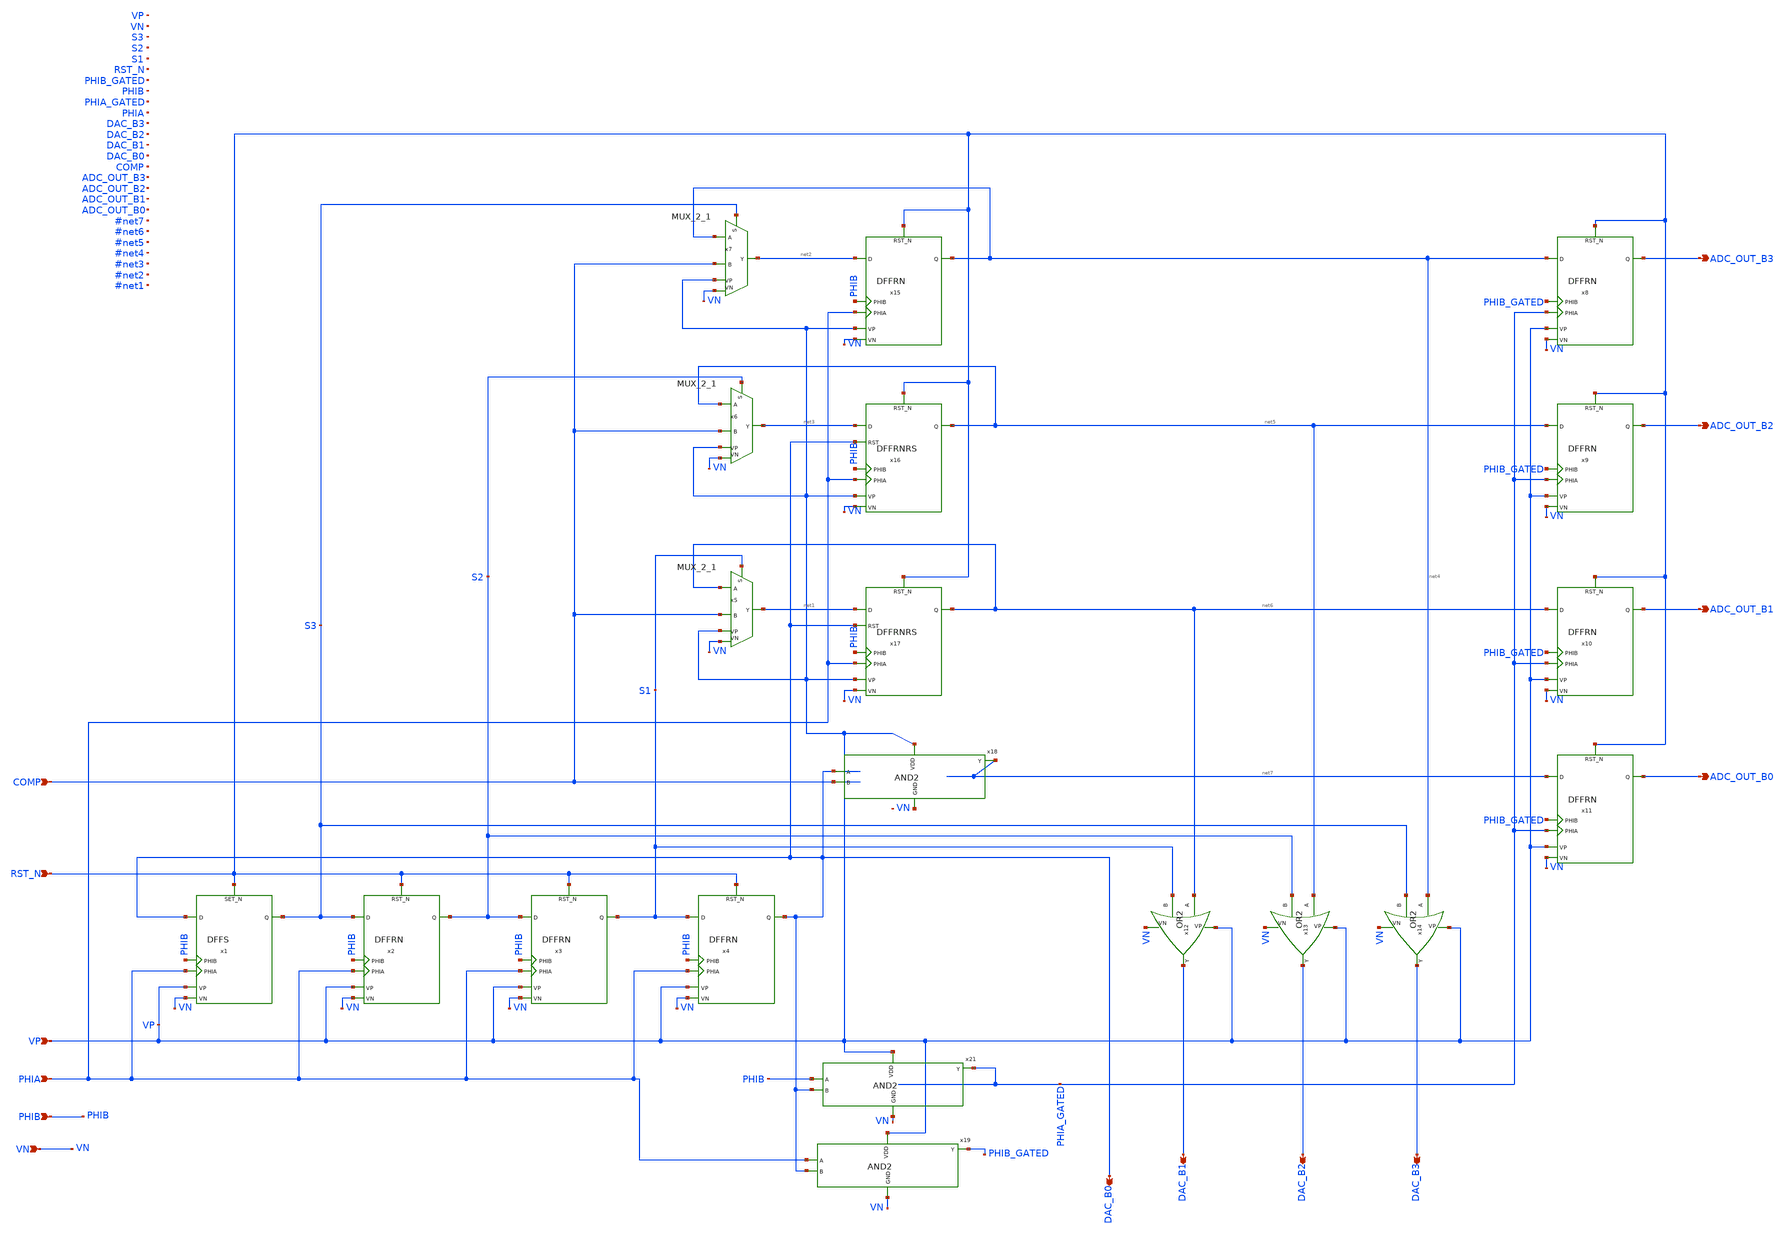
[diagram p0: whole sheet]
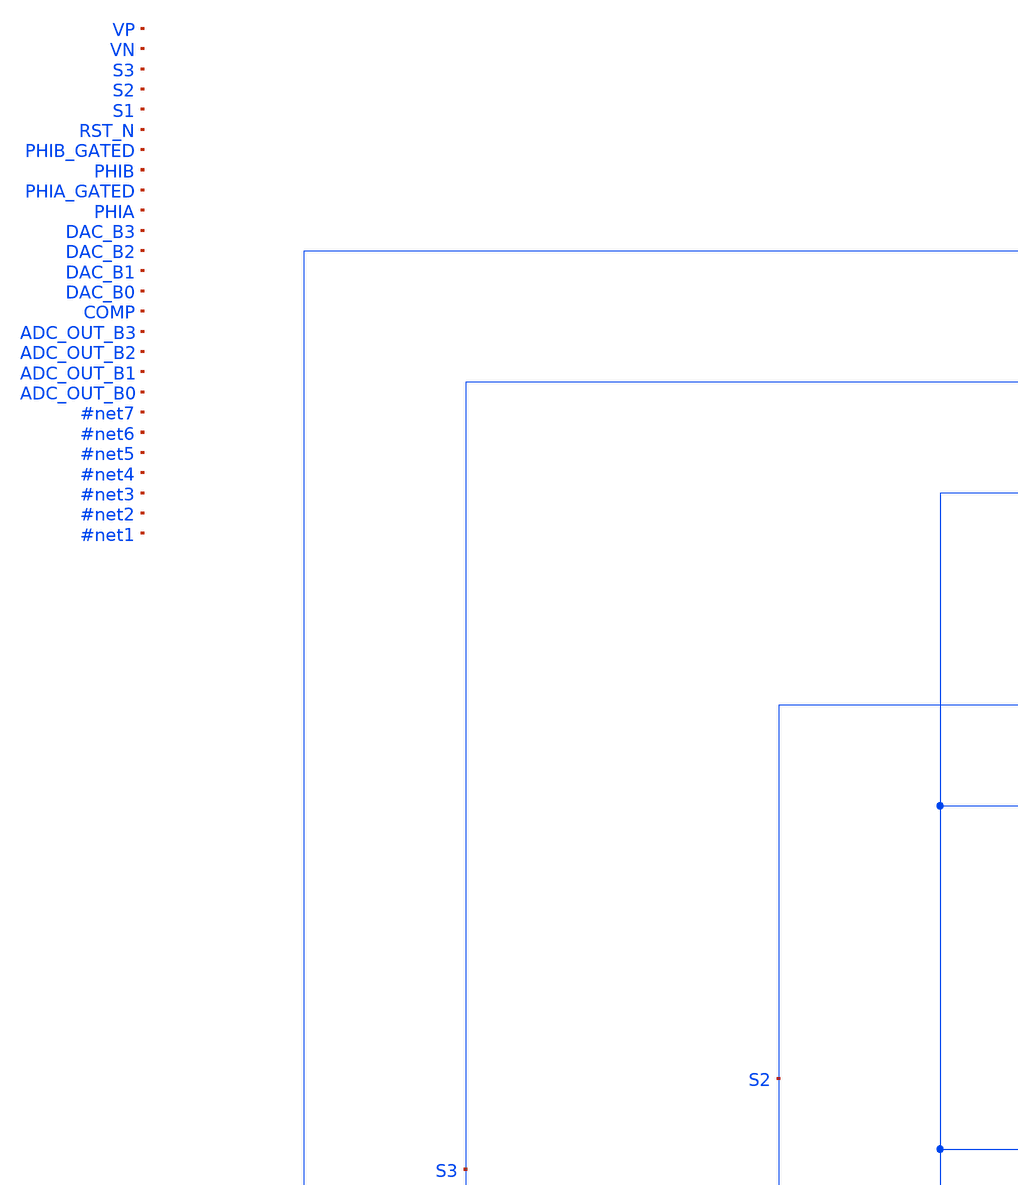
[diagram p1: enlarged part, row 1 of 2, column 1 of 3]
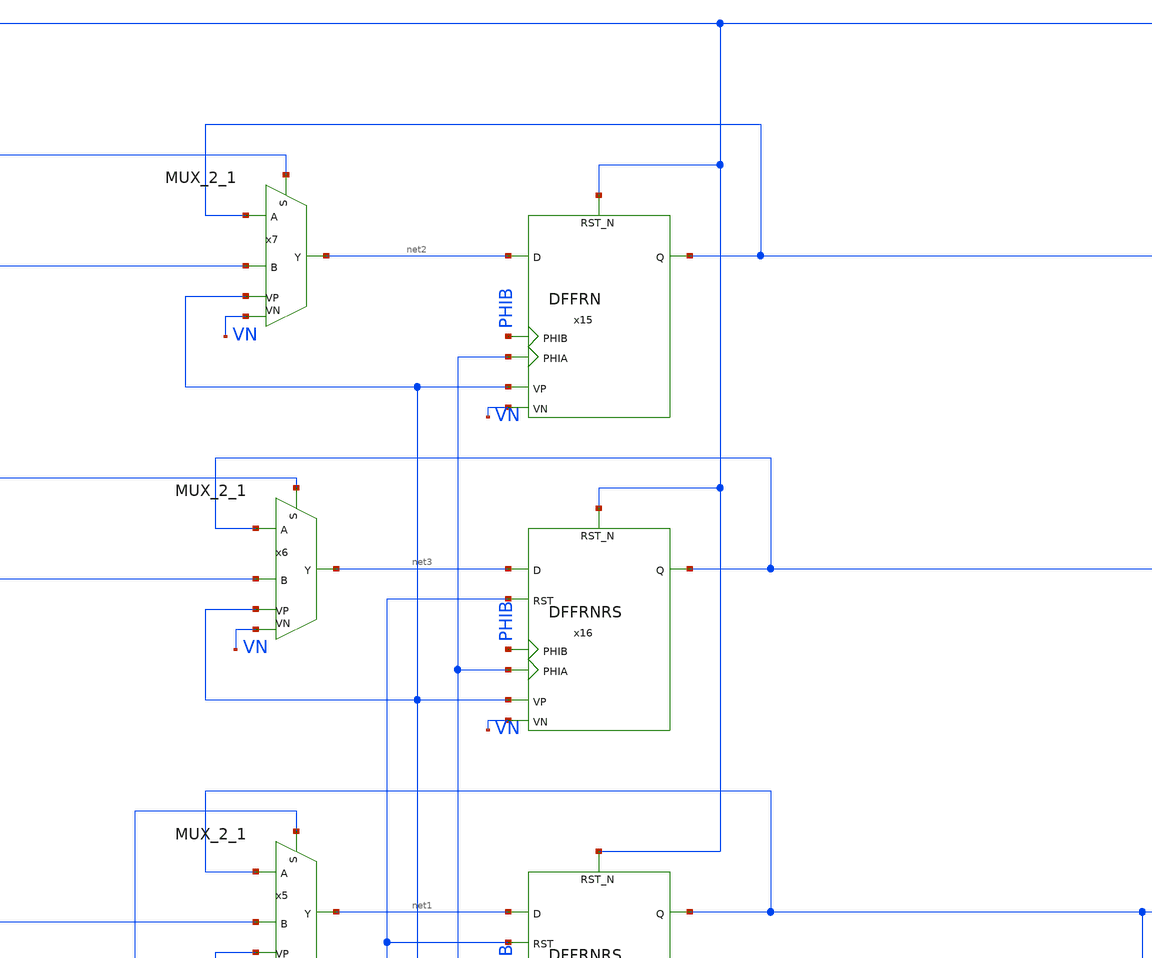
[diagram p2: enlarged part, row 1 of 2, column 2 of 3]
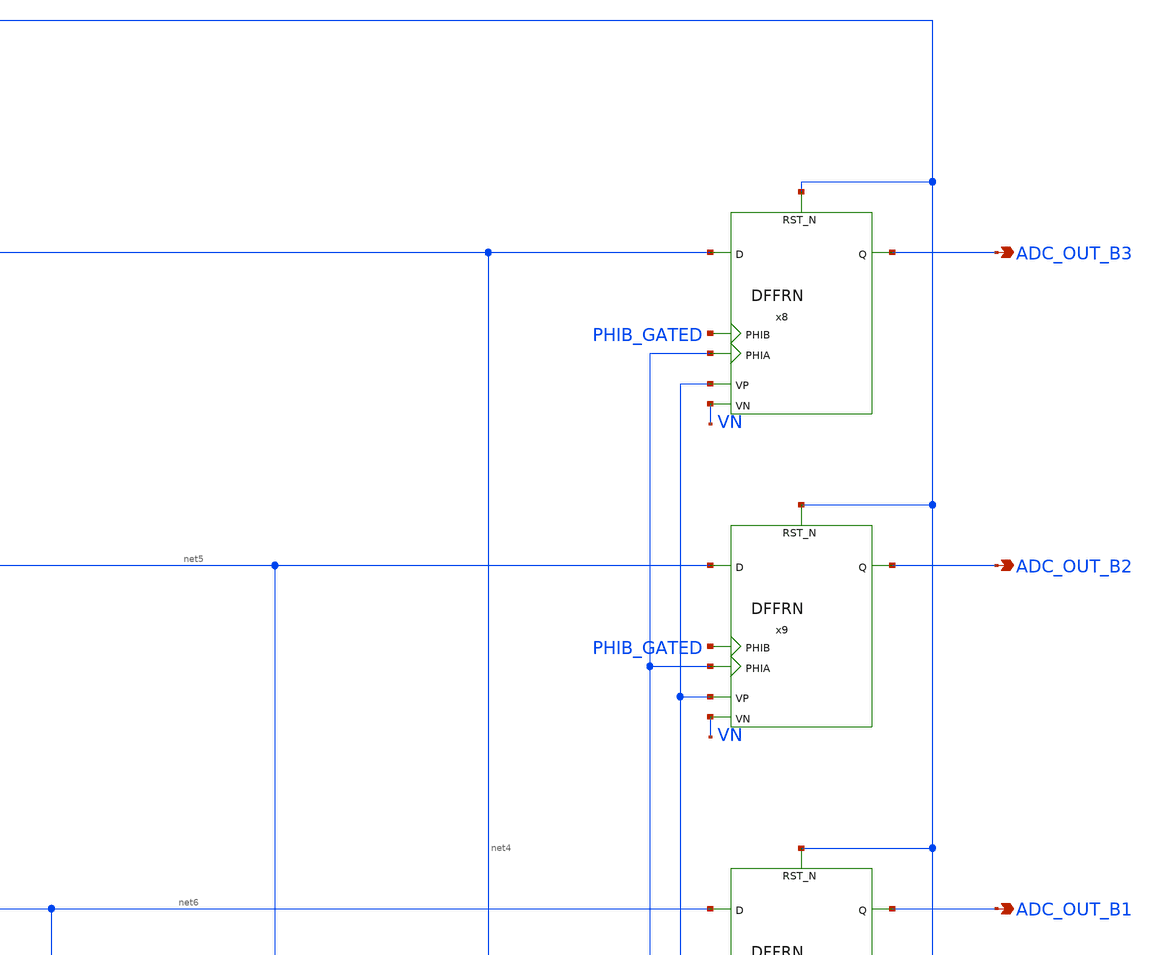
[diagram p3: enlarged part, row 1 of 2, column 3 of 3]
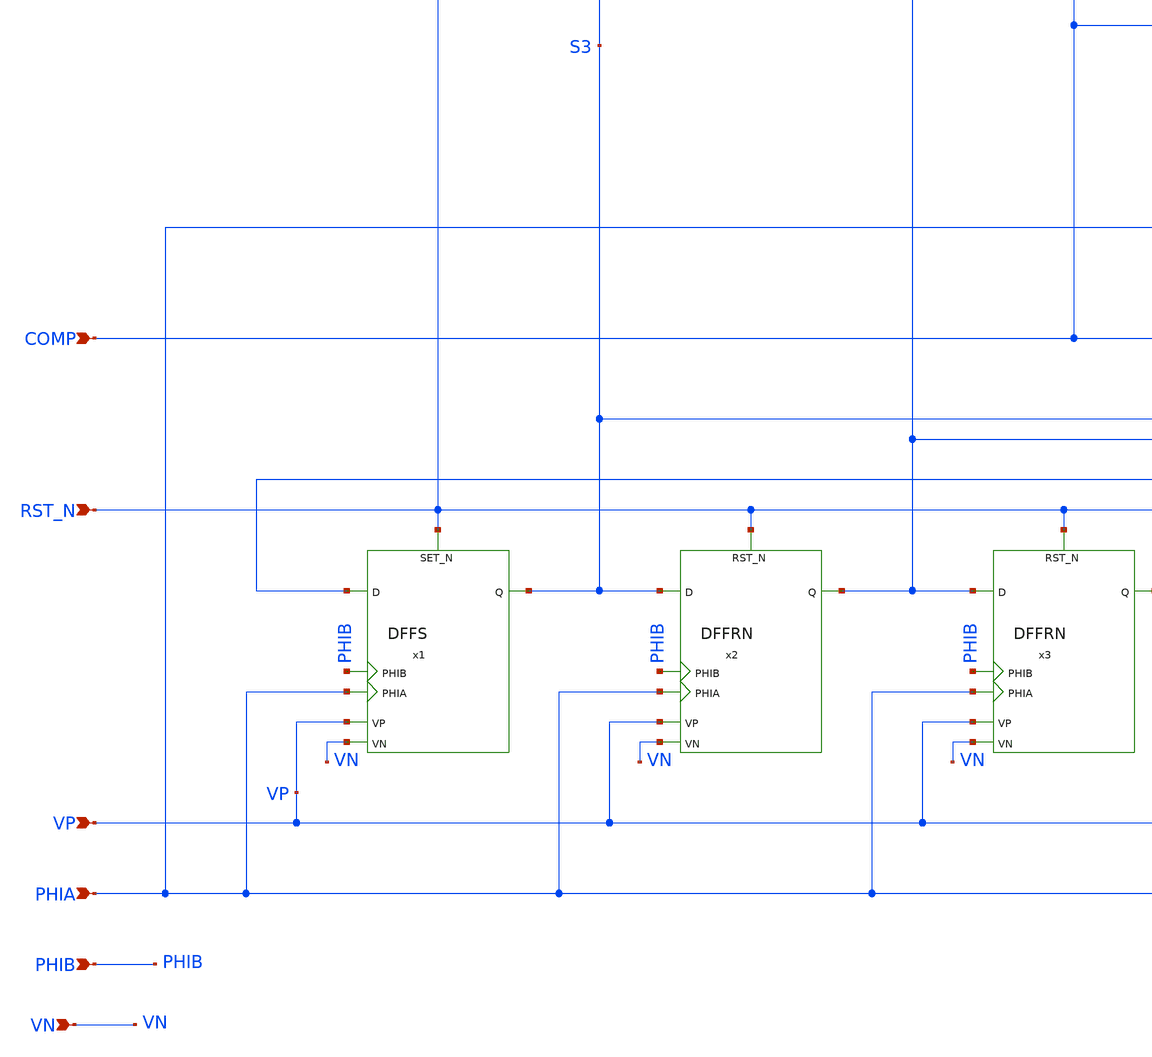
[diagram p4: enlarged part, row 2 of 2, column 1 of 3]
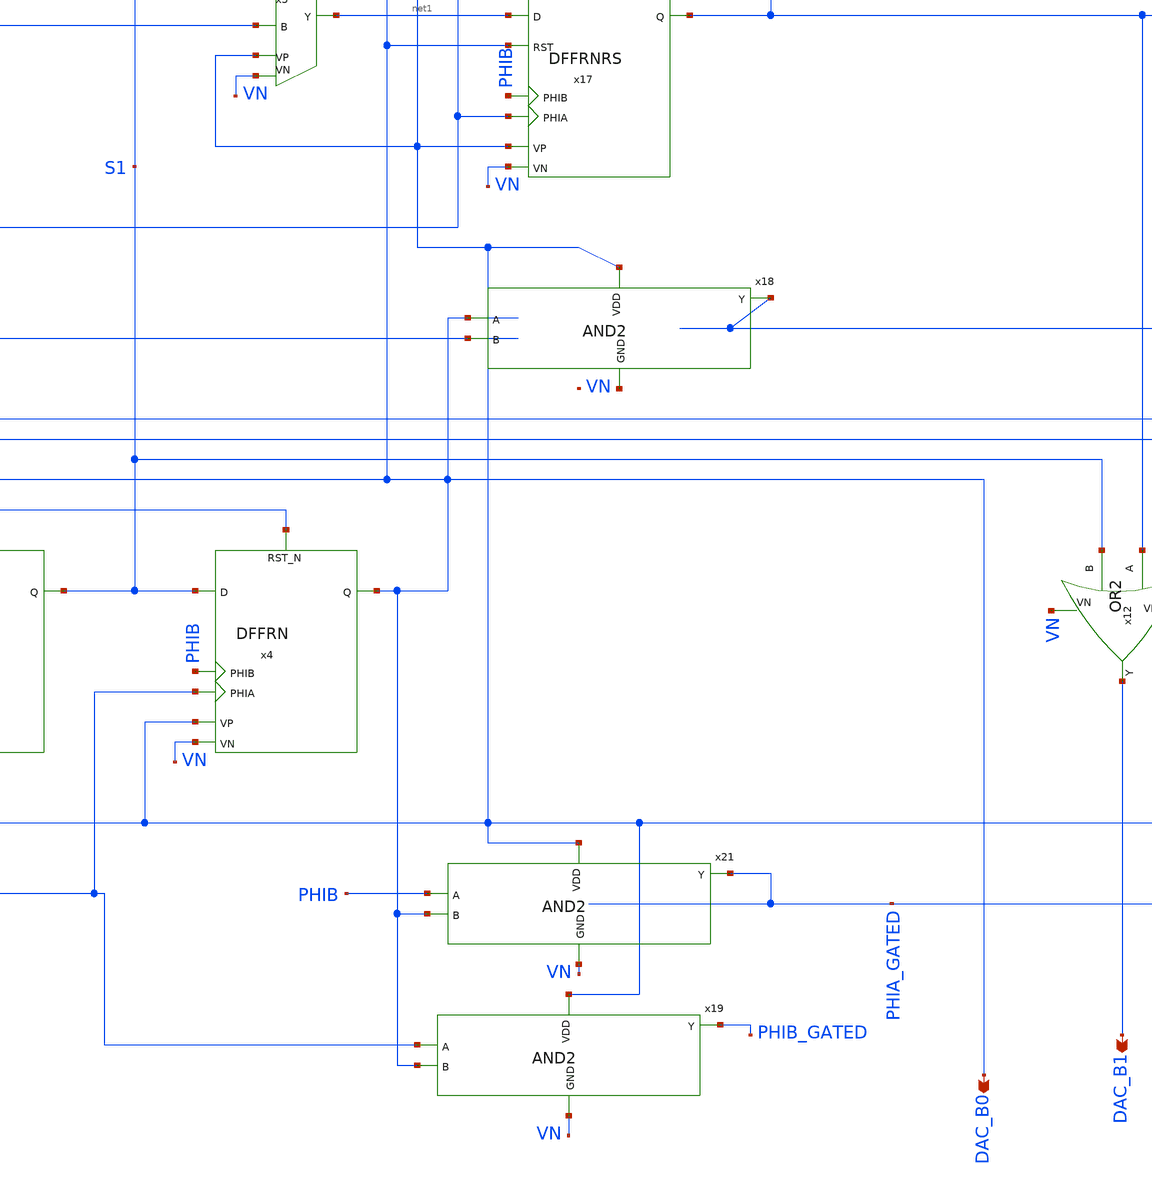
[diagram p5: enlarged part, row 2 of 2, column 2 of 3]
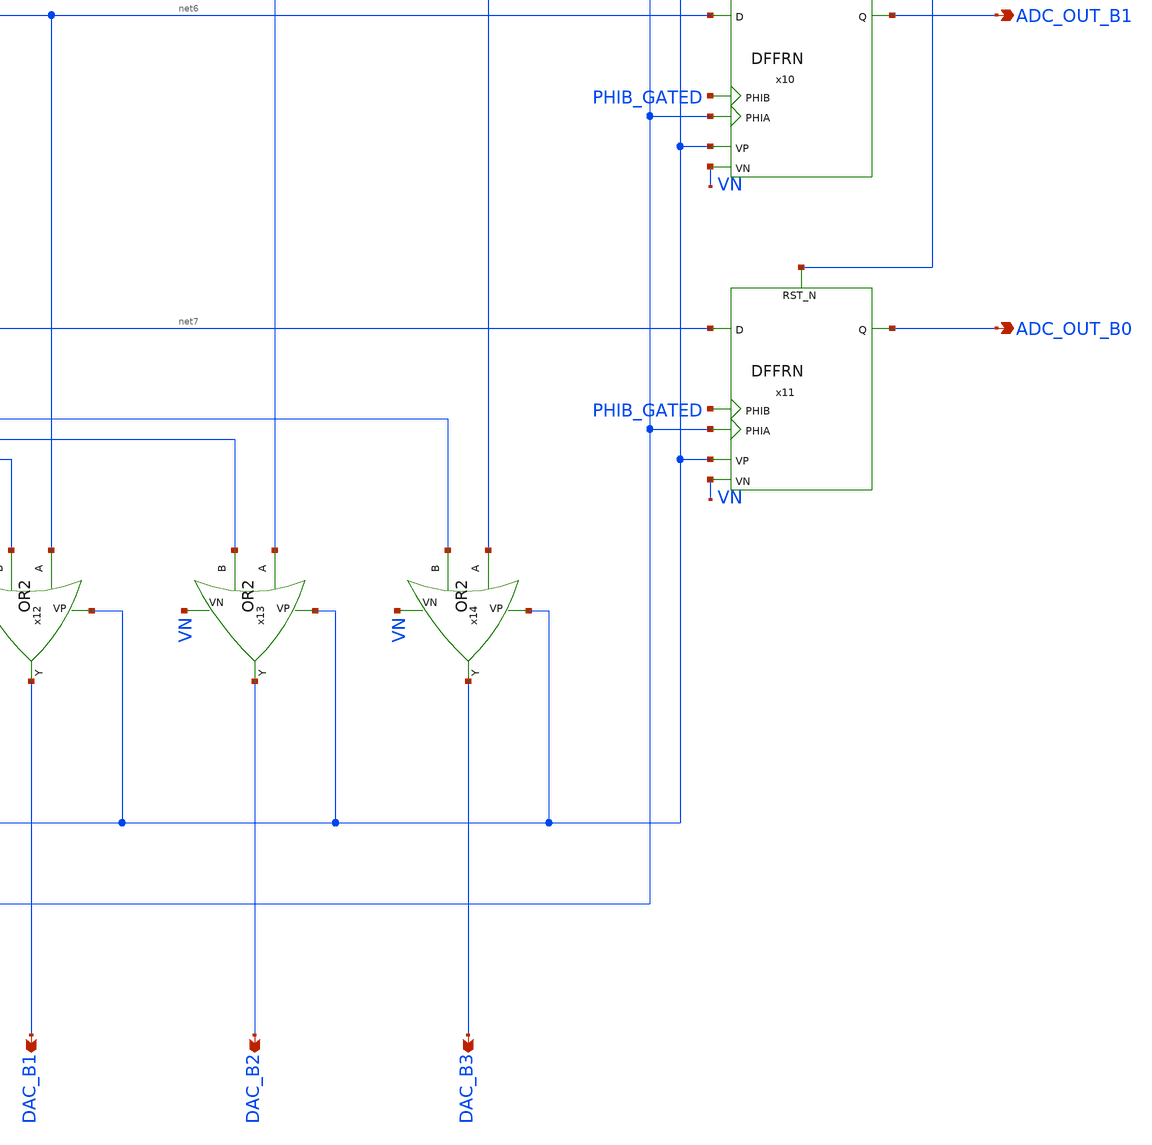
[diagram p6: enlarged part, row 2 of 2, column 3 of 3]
** sch_path: ADC/16bit_C2C/MagicAndSpice/EE431_FinalProj/SAR.sch
**.subckt SAR RST_N COMP VP PHIA ADC_OUT_B2 ADC_OUT_B3 ADC_OUT_B1 ADC_OUT_B0 DAC_B0 DAC_B1 DAC_B2
*+ DAC_B3 PHIB VN
*.ipin RST_N
*.ipin COMP
*.ipin VP
*.ipin PHIA
*.opin ADC_OUT_B2
*.opin ADC_OUT_B3
*.opin ADC_OUT_B1
*.opin ADC_OUT_B0
*.opin DAC_B0
*.opin DAC_B1
*.opin DAC_B2
*.opin DAC_B3
*.ipin PHIB
*.ipin VN
x2 PHIA PHIB S3 S2 RST_N VP VN DFFRN
x3 PHIA PHIB S2 S1 RST_N VP VN DFFRN
x4 PHIA PHIB S1 DAC_B0 RST_N VP VN DFFRN
x12 net6 S1 DAC_B1 VP VN OR2
x13 net5 S2 DAC_B2 VP VN OR2
x14 net4 S3 DAC_B3 VP VN OR2
x15 PHIA PHIB net2 net4 RST_N VP VN DFFRN
x16 PHIA PHIB net3 net5 RST_N DAC_B0 VP VN DFFRNRS
x17 PHIA PHIB net1 net6 RST_N DAC_B0 VP VN DFFRNRS
x18 VP net7 DAC_B0 COMP net8 AND2
x1 PHIA PHIB DAC_B0 S3 RST_N VP VN DFFS
x5 net6 COMP S1 net1 VP VN MUX_2_1
x6 net5 COMP S2 net3 VP VN MUX_2_1
x7 net4 COMP S3 net2 VP VN MUX_2_1
x8 PHIA_GATED PHIB_GATED net4 ADC_OUT_B3 RST_N VP VN DFFRN
x9 PHIA_GATED PHIB_GATED net5 ADC_OUT_B2 RST_N VP VN DFFRN
x10 PHIA_GATED PHIB_GATED net6 ADC_OUT_B1 RST_N VP VN DFFRN
x11 PHIA_GATED PHIB_GATED net7 ADC_OUT_B0 RST_N VP VN DFFRN
x21 VP PHIA_GATED PHIB DAC_B0 VN AND2
x19 VP PHIB_GATED PHIA DAC_B0 VN AND2
**.ends
.end
